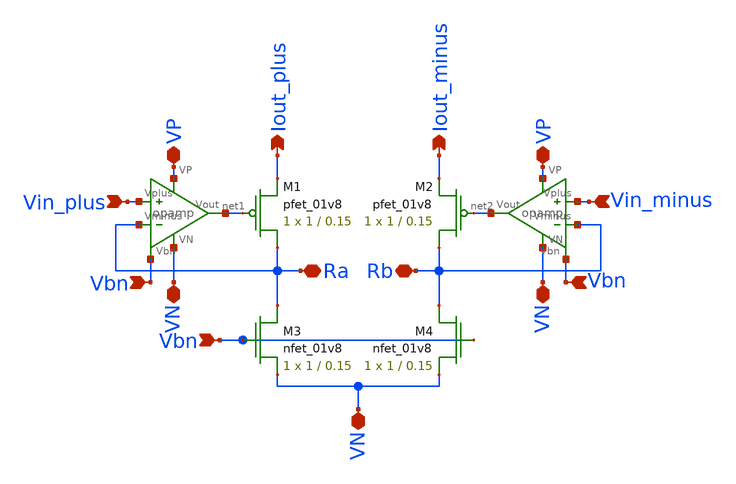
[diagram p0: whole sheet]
** sch_path: final/schematics/VI_input.sch
**.subckt VI_input VP VN VN VN VP Ra Rb Vbn Vbn Vbn Vin_plus Vin_minus Iout_plus Iout_minus
*.iopin VP
*.iopin VN
*.iopin VN
*.iopin VN
*.iopin VP
*.iopin Ra
*.iopin Rb
*.ipin Vbn
*.ipin Vbn
*.ipin Vbn
*.ipin Vin_plus
*.ipin Vin_minus
*.opin Iout_plus
*.opin Iout_minus
XM1 Ra net1 Iout_plus VDD sky130_fd_pr__pfet_01v8 L=0.15 W=1 nf=1 ad='int((nf+1)/2) * W/nf * 0.29' as='int((nf+2)/2) * W/nf * 0.29'
+ pd='2*int((nf+1)/2) * (W/nf + 0.29)' ps='2*int((nf+2)/2) * (W/nf + 0.29)' nrd='0.29 / W' nrs='0.29 / W'
+ sa=0 sb=0 sd=0 mult=1 m=1
XM2 Rb net2 Iout_minus VDD sky130_fd_pr__pfet_01v8 L=0.15 W=1 nf=1 ad='int((nf+1)/2) * W/nf * 0.29' as='int((nf+2)/2) * W/nf * 0.29'
+ pd='2*int((nf+1)/2) * (W/nf + 0.29)' ps='2*int((nf+2)/2) * (W/nf + 0.29)' nrd='0.29 / W' nrs='0.29 / W'
+ sa=0 sb=0 sd=0 mult=1 m=1
X2 net2 VP VN Vin_minus Rb Vbn opamp
XM3 Ra Vbn VN GND sky130_fd_pr__nfet_01v8 L=0.15 W=1 nf=1 ad='int((nf+1)/2) * W/nf * 0.29' as='int((nf+2)/2) * W/nf * 0.29'
+ pd='2*int((nf+1)/2) * (W/nf + 0.29)' ps='2*int((nf+2)/2) * (W/nf + 0.29)' nrd='0.29 / W' nrs='0.29 / W'
+ sa=0 sb=0 sd=0 mult=1 m=1
XM4 Rb Vbn VN GND sky130_fd_pr__nfet_01v8 L=0.15 W=1 nf=1 ad='int((nf+1)/2) * W/nf * 0.29' as='int((nf+2)/2) * W/nf * 0.29'
+ pd='2*int((nf+1)/2) * (W/nf + 0.29)' ps='2*int((nf+2)/2) * (W/nf + 0.29)' nrd='0.29 / W' nrs='0.29 / W'
+ sa=0 sb=0 sd=0 mult=1 m=1
X1 net1 VP VN Vin_plus Ra Vbn opamp
**.ends

* expanding   symbol:  opamp.sym # of pins=6
** sym_path: final/schematics/opamp.sym
** sch_path: final/schematics/opamp.sch
.subckt opamp Vout VP VN Vplus Vminus Vbn
*.iopin VP
*.iopin VN
*.ipin Vplus
*.ipin Vminus
*.opin Vout
*.ipin Vbn
XM1 net1 Vplus net2 GND sky130_fd_pr__nfet_01v8 L=0.15 W=1 nf=1 ad='int((nf+1)/2) * W/nf * 0.29' as='int((nf+2)/2) * W/nf * 0.29'
+ pd='2*int((nf+1)/2) * (W/nf + 0.29)' ps='2*int((nf+2)/2) * (W/nf + 0.29)' nrd='0.29 / W' nrs='0.29 / W'
+ sa=0 sb=0 sd=0 mult=1 m=1
XM2 Vout Vminus net2 GND sky130_fd_pr__nfet_01v8 L=0.15 W=1 nf=1 ad='int((nf+1)/2) * W/nf * 0.29' as='int((nf+2)/2) * W/nf * 0.29'
+ pd='2*int((nf+1)/2) * (W/nf + 0.29)' ps='2*int((nf+2)/2) * (W/nf + 0.29)' nrd='0.29 / W' nrs='0.29 / W'
+ sa=0 sb=0 sd=0 mult=1 m=1
XM3 net2 Vbn VN GND sky130_fd_pr__nfet_01v8 L=0.15 W=1 nf=1 ad='int((nf+1)/2) * W/nf * 0.29' as='int((nf+2)/2) * W/nf * 0.29'
+ pd='2*int((nf+1)/2) * (W/nf + 0.29)' ps='2*int((nf+2)/2) * (W/nf + 0.29)' nrd='0.29 / W' nrs='0.29 / W'
+ sa=0 sb=0 sd=0 mult=1 m=1
XM4 net1 net1 VP VDD sky130_fd_pr__pfet_01v8 L=0.15 W=1 nf=1 ad='int((nf+1)/2) * W/nf * 0.29' as='int((nf+2)/2) * W/nf * 0.29'
+ pd='2*int((nf+1)/2) * (W/nf + 0.29)' ps='2*int((nf+2)/2) * (W/nf + 0.29)' nrd='0.29 / W' nrs='0.29 / W'
+ sa=0 sb=0 sd=0 mult=1 m=1
XM5 Vout net1 VP VDD sky130_fd_pr__pfet_01v8 L=0.15 W=1 nf=1 ad='int((nf+1)/2) * W/nf * 0.29' as='int((nf+2)/2) * W/nf * 0.29'
+ pd='2*int((nf+1)/2) * (W/nf + 0.29)' ps='2*int((nf+2)/2) * (W/nf + 0.29)' nrd='0.29 / W' nrs='0.29 / W'
+ sa=0 sb=0 sd=0 mult=1 m=1
.ends

.end
